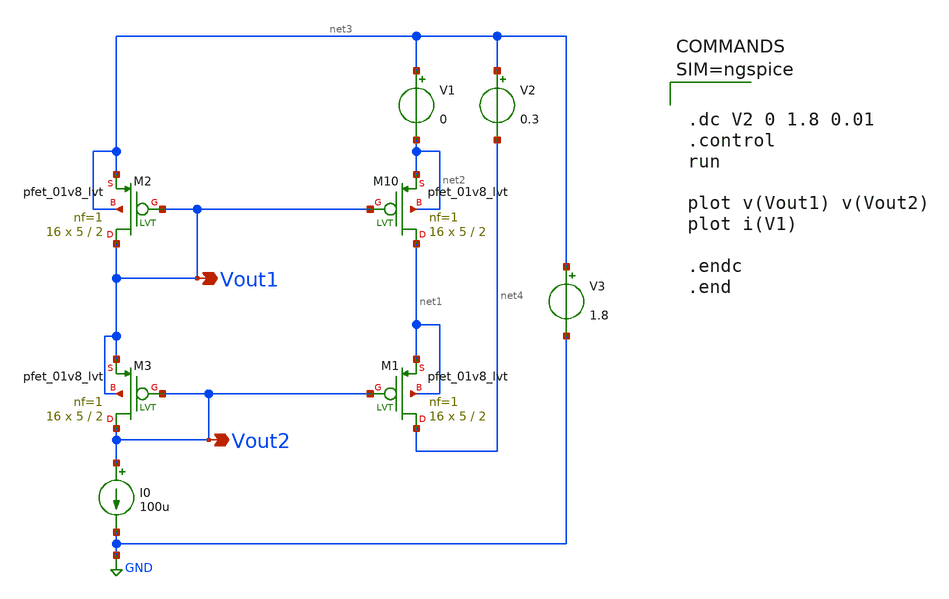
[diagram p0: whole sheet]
** sch_path: sch/Cascaded_curr_mirr_PMOS.sch
**.subckt Cascaded_curr_mirr_PMOS Vout1 Vout2
*.opin Vout1
*.opin Vout2
XM10 net1 Vout1 net2 net2 sky130_fd_pr__pfet_01v8_lvt L=2 W=5 nf=1 ad='int((1 + 1)/2) * 5 / 1 * 0.29'
+ as='int((1 + 2)/2) * 5 / 1 * 0.29' pd='2*int((1 + 1)/2) * (5 / 1 + 0.29)' ps='2*int((1 + 2)/2) * (5 / 1 + 0.29)'
+ nrd='0.29 / 5 ' nrs='0.29 / 5 ' sa=0 sb=0 sd=0 mult=16 m=16
XM1 net4 Vout2 net1 net1 sky130_fd_pr__pfet_01v8_lvt L=2 W=5 nf=1 ad='int((1 + 1)/2) * 5 / 1 * 0.29'
+ as='int((1 + 2)/2) * 5 / 1 * 0.29' pd='2*int((1 + 1)/2) * (5 / 1 + 0.29)' ps='2*int((1 + 2)/2) * (5 / 1 + 0.29)'
+ nrd='0.29 / 5 ' nrs='0.29 / 5 ' sa=0 sb=0 sd=0 mult=16 m=16
XM2 Vout1 Vout1 net3 net3 sky130_fd_pr__pfet_01v8_lvt L=2 W=5 nf=1 ad='int((1 + 1)/2) * 5 / 1 * 0.29'
+ as='int((1 + 2)/2) * 5 / 1 * 0.29' pd='2*int((1 + 1)/2) * (5 / 1 + 0.29)' ps='2*int((1 + 2)/2) * (5 / 1 + 0.29)'
+ nrd='0.29 / 5 ' nrs='0.29 / 5 ' sa=0 sb=0 sd=0 mult=16 m=16
XM3 Vout2 Vout2 Vout1 Vout1 sky130_fd_pr__pfet_01v8_lvt L=2 W=5 nf=1 ad='int((1 + 1)/2) * 5 / 1 * 0.29'
+ as='int((1 + 2)/2) * 5 / 1 * 0.29' pd='2*int((1 + 1)/2) * (5 / 1 + 0.29)' ps='2*int((1 + 2)/2) * (5 / 1 + 0.29)'
+ nrd='0.29 / 5 ' nrs='0.29 / 5 ' sa=0 sb=0 sd=0 mult=16 m=16
I0 Vout2 GND 100u
V3 net3 GND 1.8
V1 net3 net2 0
V2 net3 net4 0.3
**** begin user architecture code

** opencircuitdesign pdks install
.lib $::SKYWATER_MODELS/sky130.lib.spice tt




.dc V2 0 1.8 0.01
.control
run

plot v(Vout1) v(Vout2)
plot i(V1)

.endc
.end



**** end user architecture code
**.ends
.GLOBAL GND
.end
